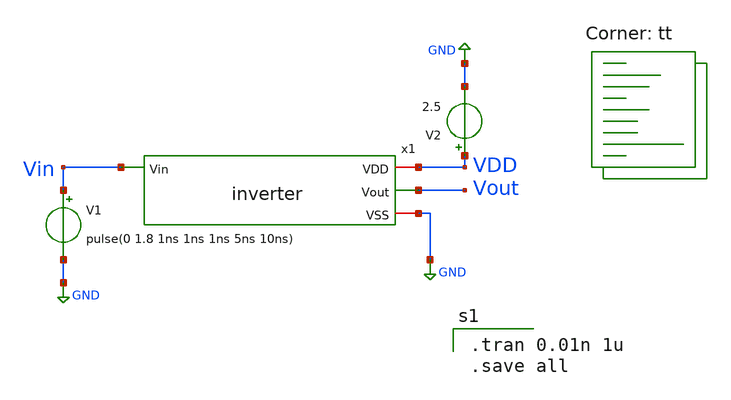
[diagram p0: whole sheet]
** sch_path: analog/schematics/testbenches/inverter_tb.sch
**.subckt inverter_tb
x1 VDD Vout Vin GND inverter
V1 Vin GND pulse(0 1.8 1ns 1ns 1ns 5ns 10ns)
V2 VDD GND 2.5
**** begin user architecture code

.tran 0.01n 1u
.save all

.lib $::SKYWATER_MODELS/sky130.lib.spice tt
**** end user architecture code
**.ends
.GLOBAL GND
.end
